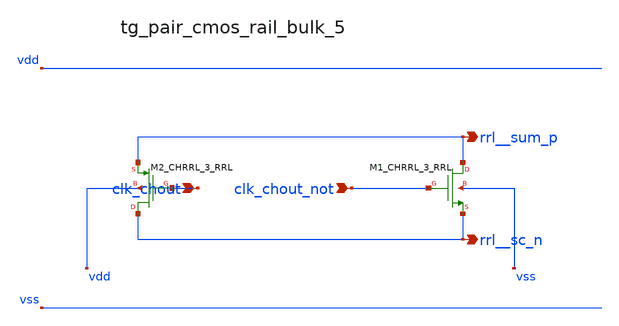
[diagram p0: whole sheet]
** sch_path: analog-db/raw/ia_004_fan_chopper_rrl/hier/blocks/tg_pair_cmos_rail_bulk_5.sch
**.subckt tg_pair_cmos_rail_bulk_5 clk_chout clk_chout_not rrl__sum_p rrl__sc_n
*.ipin clk_chout
*.ipin clk_chout_not
*.opin rrl__sum_p
*.opin rrl__sc_n
XM1_CHRRL_3_RRL rrl__sum_p clk_chout_not rrl__sc_n vss sg13_lv_nmos w=x_dut_xm1_chrrl_3_rrl_w
+ l=x_dut_xm1_chrrl_3_rrl_l ng=1 m=x_dut_xm1_chrrl_3_rrl_m
XM2_CHRRL_3_RRL rrl__sc_n clk_chout rrl__sum_p vdd sg13_lv_pmos w=x_dut_xm2_chrrl_3_rrl_w
+ l=x_dut_xm2_chrrl_3_rrl_l ng=1 m=x_dut_xm2_chrrl_3_rrl_m
**.ends
.end
